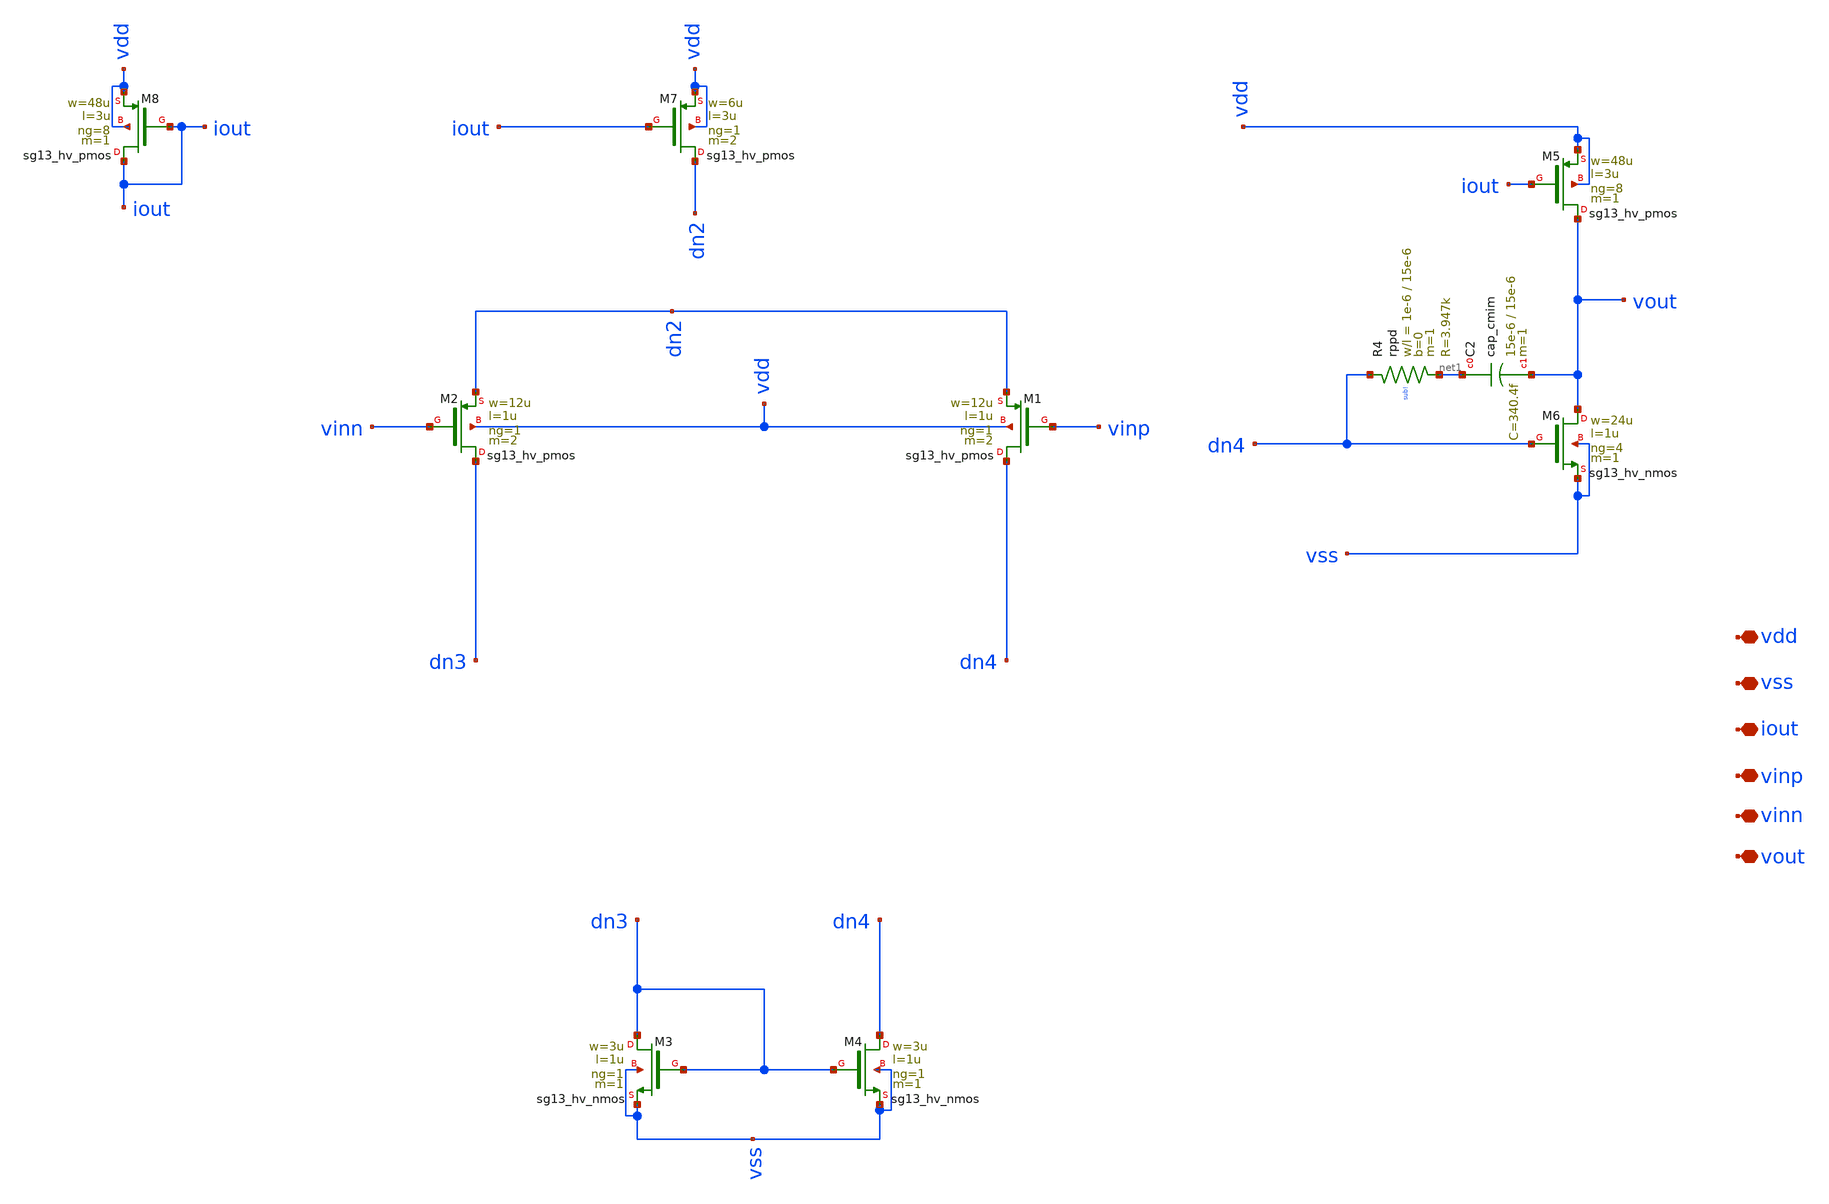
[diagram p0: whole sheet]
** sch_path: dependencies/pmu_ip/dependencies/OTA/OTA-main/netlist/pex/tb/ota_layout.sch
**.subckt ota_layout vdd vss iout vinp vinn vout
*.iopin vdd
*.iopin vss
*.iopin iout
*.iopin vinp
*.iopin vinn
*.iopin vout
XM1 dn4 vinp dn2 vdd sg13_hv_pmos w=12u l=1u ng=1 m=2 mm_ok=1
XM2 dn3 vinn dn2 vdd sg13_hv_pmos w=12u l=1u ng=1 m=2 mm_ok=1
XC2 net1 vout cap_cmim w=15e-6 l=15e-6 m=1 mm_ok=1
XR4 dn4 net1 sub! rppd w=1e-6 l=15e-6 m=1 b=0 mm_ok=1
XM5 vout iout vdd vdd sg13_hv_pmos w=48u l=3u ng=8 m=1 mm_ok=1
XM6 vout dn4 vss vss sg13_hv_nmos w=24u l=1u ng=4 m=1 mm_ok=1
XM7 dn2 iout vdd vdd sg13_hv_pmos w=6u l=3u ng=1 m=2 mm_ok=1
XM8 iout iout vdd vdd sg13_hv_pmos w=48u l=3u ng=8 m=1 mm_ok=1
XM3 dn3 dn3 vss vss sg13_hv_nmos w=3u l=1u ng=1 m=1 mm_ok=1
XM4 dn4 dn3 vss vss sg13_hv_nmos w=3u l=1u ng=1 m=1 mm_ok=1
**.ends
.end
